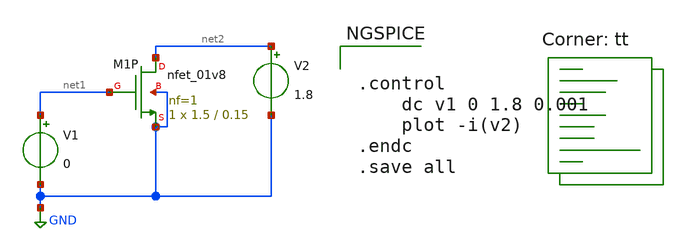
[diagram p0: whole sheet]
** sch_path: parametros.sch
**.subckt parametros
V1 net1 GND 0
V2 net2 GND 1.8
XM1P net2 net1 GND GND sky130_fd_pr__nfet_01v8 L=0.15 W=1.5 nf=1 ad='int((nf+1)/2) * W/nf * 0.29' as='int((nf+2)/2) * W/nf * 0.29'
+ pd='2*int((nf+1)/2) * (W/nf + 0.29)' ps='2*int((nf+2)/2) * (W/nf + 0.29)' nrd='0.29 / W' nrs='0.29 / W'
+ sa=0 sb=0 sd=0 mult=1 m=1
**** begin user architecture code


.control
	dc v1 0 1.8 0.001
	plot -i(v2)
.endc
.save all


.lib $::SKYWATER_MODELS/sky130.lib.spice tt
**** end user architecture code
**.ends
.GLOBAL GND
.end
